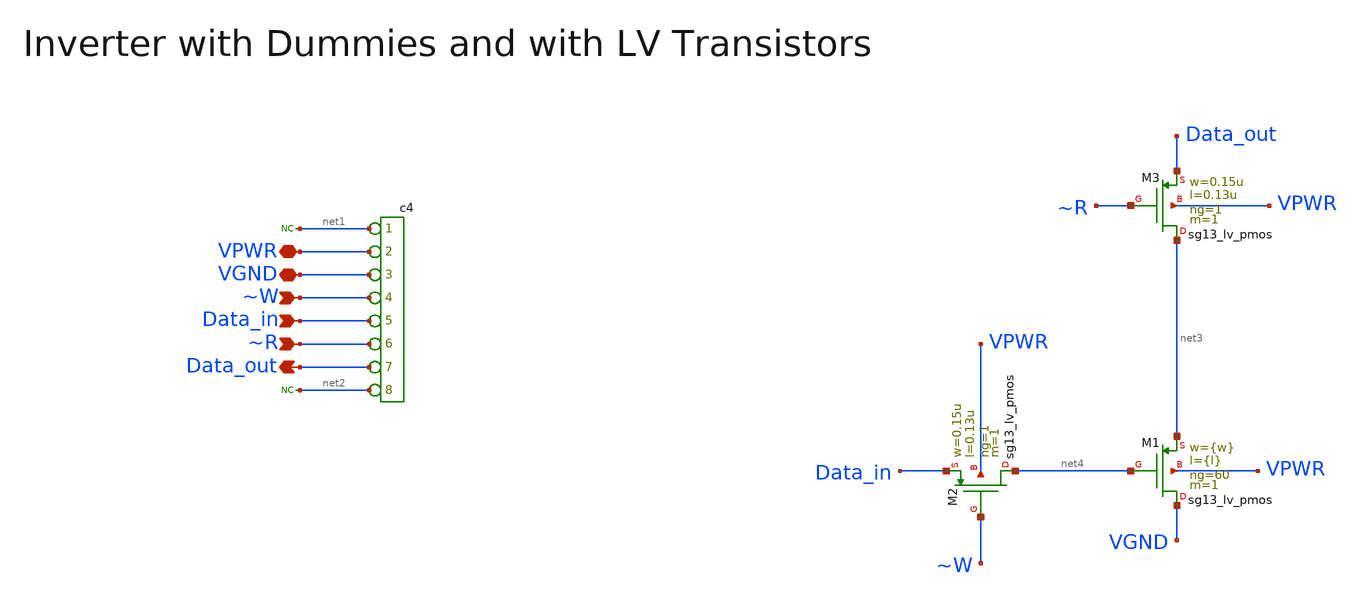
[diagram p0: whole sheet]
** sch_path: macros/heichips26_analog_project/macros/dramcell/schematic/xschem/dramcell.sch
**.subckt dramcell Data_out ~W Data_in ~R VPWR VGND
*.opin Data_out
*.ipin ~W
*.ipin Data_in
*.ipin ~R
*.iopin VPWR
*.iopin VGND
XM2 net4 ~W Data_in VPWR sg13_lv_pmos w=0.15u l=0.13u ng=1 m=1 mm_ok=1
XM3 net3 ~R Data_out VPWR sg13_lv_pmos w=0.15u l=0.13u ng=1 m=1 mm_ok=1
XM1 VGND net4 net3 VPWR sg13_lv_pmos w={w} l={l} ng=60 m=1 mm_ok=1
*connector(8,1) ?1 net1 ?1 VPWR ?1 VGND ?1 ~W ?1 Data_in ?1 ~R ?1 Data_out ?1 net2
* noconn #net1
* noconn #net2
**.ends
.end
